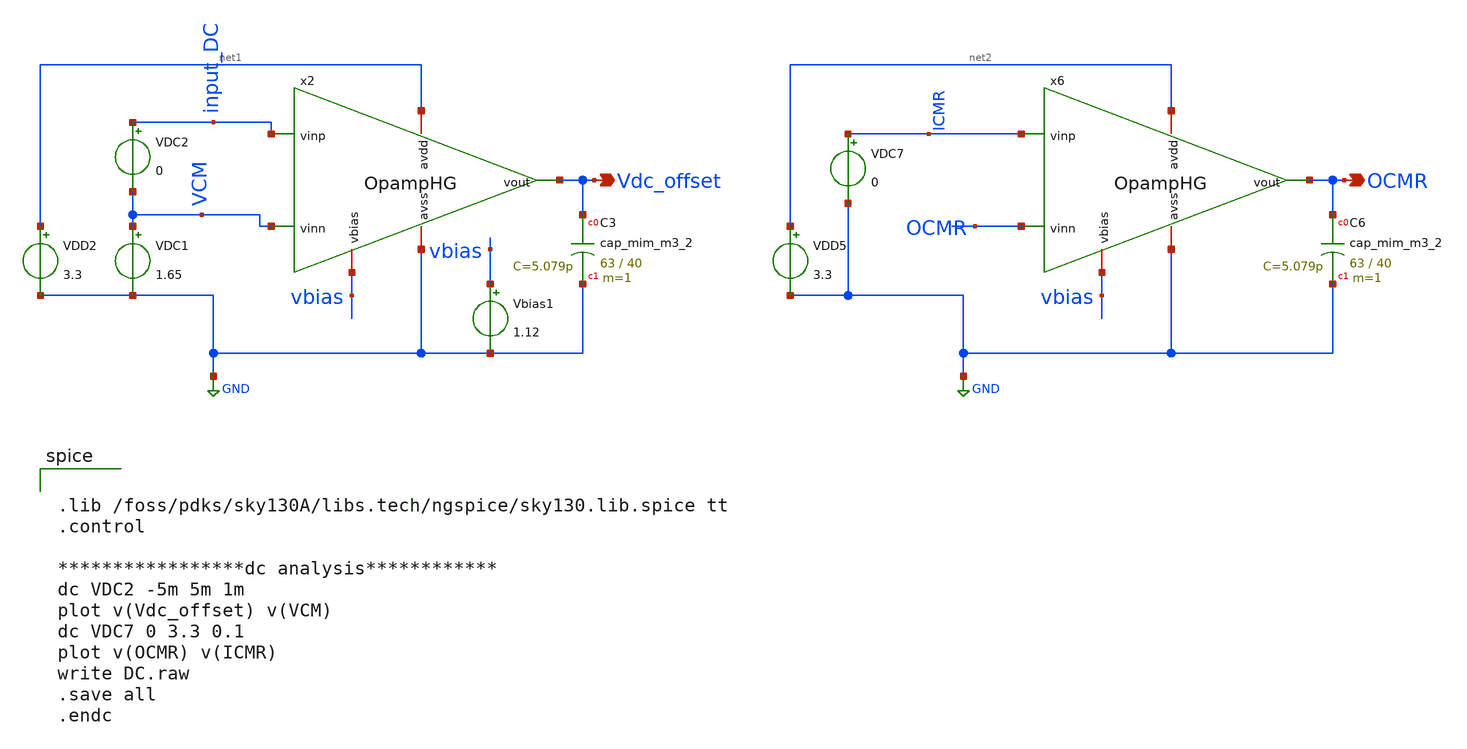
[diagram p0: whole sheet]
** sch_path: OpampHG_DC.sch
**.subckt OpampHG_DC Vdc_offset OCMR
*.opin Vdc_offset
*.opin OCMR
x2 net1 GND vbias input_DC VCM Vdc_offset OpampHG
VDD2 net1 GND 3.3
VDC1 VCM GND 1.65
XC3 Vdc_offset GND sky130_fd_pr__cap_mim_m3_2 W=63 L=40 MF=1 m=1
VDC2 input_DC VCM 0
x6 net2 GND vbias ICMR OCMR OCMR OpampHG
VDD5 net2 GND 3.3
VDC7 ICMR GND 0
XC6 OCMR GND sky130_fd_pr__cap_mim_m3_2 W=63 L=40 MF=1 m=1
Vbias1 vbias GND 1.12
**** begin user architecture code


.lib /foss/pdks/sky130A/libs.tech/ngspice/sky130.lib.spice tt
.control

*****************dc analysis************
dc VDC2 -5m 5m 1m
plot v(Vdc_offset) v(VCM)
dc VDC7 0 3.3 0.1
plot v(OCMR) v(ICMR)
write DC.raw
.save all
.endc


**** end user architecture code
**.ends

* expanding   symbol:  /foss/designs/Opamp_HG/OpampHG.sym # of pins=6
** sym_path: OpampHG.sym
** sch_path: OpampHG.sch
.subckt OpampHG avdd avss vbias vinp vinn vout
*.iopin avdd
*.iopin avss
*.iopin vbias
*.ipin vinp
*.ipin vinn
*.opin vout
XC1 net2 Vout_prior sky130_fd_pr__cap_mim_m3_1 W=13 L=9.9 MF=1 m=1
XC2 net3 vout sky130_fd_pr__cap_mim_m3_2 W=20 L=37 MF=1 m=1
XM1 net1 net2 avdd avdd sky130_fd_pr__pfet_01v8 L=0.3 W=5 nf=1 ad='int((nf+1)/2) * W/nf * 0.29' as='int((nf+2)/2) * W/nf * 0.29'
+ pd='2*int((nf+1)/2) * (W/nf + 0.29)' ps='2*int((nf+2)/2) * (W/nf + 0.29)' nrd='0.29 / W' nrs='0.29 / W'
+ sa=0 sb=0 sd=0 mult=1 m=1
XM2 net3 net2 avdd avdd sky130_fd_pr__pfet_01v8 L=0.3 W=5 nf=1 ad='int((nf+1)/2) * W/nf * 0.29' as='int((nf+2)/2) * W/nf * 0.29'
+ pd='2*int((nf+1)/2) * (W/nf + 0.29)' ps='2*int((nf+2)/2) * (W/nf + 0.29)' nrd='0.29 / W' nrs='0.29 / W'
+ sa=0 sb=0 sd=0 mult=1 m=1
XM3 net2 net2 net1 avdd sky130_fd_pr__pfet_01v8 L=0.3 W=5 nf=1 ad='int((nf+1)/2) * W/nf * 0.29' as='int((nf+2)/2) * W/nf * 0.29'
+ pd='2*int((nf+1)/2) * (W/nf + 0.29)' ps='2*int((nf+2)/2) * (W/nf + 0.29)' nrd='0.29 / W' nrs='0.29 / W'
+ sa=0 sb=0 sd=0 mult=1 m=1
XM4 net5 net2 net3 avdd sky130_fd_pr__pfet_01v8 L=0.3 W=5 nf=1 ad='int((nf+1)/2) * W/nf * 0.29' as='int((nf+2)/2) * W/nf * 0.29'
+ pd='2*int((nf+1)/2) * (W/nf + 0.29)' ps='2*int((nf+2)/2) * (W/nf + 0.29)' nrd='0.29 / W' nrs='0.29 / W'
+ sa=0 sb=0 sd=0 mult=1 m=1
XM5 net7 net6 avdd avdd sky130_fd_pr__pfet_01v8 L=0.3 W=5 nf=1 ad='int((nf+1)/2) * W/nf * 0.29' as='int((nf+2)/2) * W/nf * 0.29'
+ pd='2*int((nf+1)/2) * (W/nf + 0.29)' ps='2*int((nf+2)/2) * (W/nf + 0.29)' nrd='0.29 / W' nrs='0.29 / W'
+ sa=0 sb=0 sd=0 mult=1 m=1
XM6 net8 net6 avdd avdd sky130_fd_pr__pfet_01v8 L=0.3 W=5 nf=1 ad='int((nf+1)/2) * W/nf * 0.29' as='int((nf+2)/2) * W/nf * 0.29'
+ pd='2*int((nf+1)/2) * (W/nf + 0.29)' ps='2*int((nf+2)/2) * (W/nf + 0.29)' nrd='0.29 / W' nrs='0.29 / W'
+ sa=0 sb=0 sd=0 mult=1 m=1
XM7 net6 net6 net7 avdd sky130_fd_pr__pfet_01v8 L=0.3 W=5 nf=1 ad='int((nf+1)/2) * W/nf * 0.29' as='int((nf+2)/2) * W/nf * 0.29'
+ pd='2*int((nf+1)/2) * (W/nf + 0.29)' ps='2*int((nf+2)/2) * (W/nf + 0.29)' nrd='0.29 / W' nrs='0.29 / W'
+ sa=0 sb=0 sd=0 mult=1 m=1
XM8 Vout_prior net6 net8 avdd sky130_fd_pr__pfet_01v8 L=0.3 W=5 nf=1 ad='int((nf+1)/2) * W/nf * 0.29'
+ as='int((nf+2)/2) * W/nf * 0.29' pd='2*int((nf+1)/2) * (W/nf + 0.29)' ps='2*int((nf+2)/2) * (W/nf + 0.29)'
+ nrd='0.29 / W' nrs='0.29 / W' sa=0 sb=0 sd=0 mult=1 m=1
XM9 net11 Vout_prior avdd avdd sky130_fd_pr__pfet_01v8 L=0.3 W=50 nf=1 ad='int((nf+1)/2) * W/nf * 0.29'
+ as='int((nf+2)/2) * W/nf * 0.29' pd='2*int((nf+1)/2) * (W/nf + 0.29)' ps='2*int((nf+2)/2) * (W/nf + 0.29)'
+ nrd='0.29 / W' nrs='0.29 / W' sa=0 sb=0 sd=0 mult=1 m=1
XM10 vout Vout_prior net11 avdd sky130_fd_pr__pfet_01v8 L=0.3 W=50 nf=1 ad='int((nf+1)/2) * W/nf * 0.29'
+ as='int((nf+2)/2) * W/nf * 0.29' pd='2*int((nf+1)/2) * (W/nf + 0.29)' ps='2*int((nf+2)/2) * (W/nf + 0.29)'
+ nrd='0.29 / W' nrs='0.29 / W' sa=0 sb=0 sd=0 mult=1 m=1
XM11 net2 vinn net4 avss sky130_fd_pr__nfet_01v8 L=2 W=5 nf=1 ad='int((nf+1)/2) * W/nf * 0.29' as='int((nf+2)/2) * W/nf * 0.29'
+ pd='2*int((nf+1)/2) * (W/nf + 0.29)' ps='2*int((nf+2)/2) * (W/nf + 0.29)' nrd='0.29 / W' nrs='0.29 / W'
+ sa=0 sb=0 sd=0 mult=1 m=1
XM12 net5 vinp net4 avss sky130_fd_pr__nfet_01v8 L=2 W=5 nf=1 ad='int((nf+1)/2) * W/nf * 0.29' as='int((nf+2)/2) * W/nf * 0.29'
+ pd='2*int((nf+1)/2) * (W/nf + 0.29)' ps='2*int((nf+2)/2) * (W/nf + 0.29)' nrd='0.29 / W' nrs='0.29 / W'
+ sa=0 sb=0 sd=0 mult=1 m=1
XM13 net6 net5 net10 avss sky130_fd_pr__nfet_01v8 L=2 W=5 nf=1 ad='int((nf+1)/2) * W/nf * 0.29' as='int((nf+2)/2) * W/nf * 0.29'
+ pd='2*int((nf+1)/2) * (W/nf + 0.29)' ps='2*int((nf+2)/2) * (W/nf + 0.29)' nrd='0.29 / W' nrs='0.29 / W'
+ sa=0 sb=0 sd=0 mult=1 m=1
XM14 Vout_prior net2 net9 avss sky130_fd_pr__nfet_01v8 L=2 W=5 nf=1 ad='int((nf+1)/2) * W/nf * 0.29'
+ as='int((nf+2)/2) * W/nf * 0.29' pd='2*int((nf+1)/2) * (W/nf + 0.29)' ps='2*int((nf+2)/2) * (W/nf + 0.29)'
+ nrd='0.29 / W' nrs='0.29 / W' sa=0 sb=0 sd=0 mult=1 m=1
XM15 net4 vbias avss avss sky130_fd_pr__nfet_01v8 L=0.6 W=2.6 nf=1 ad='int((nf+1)/2) * W/nf * 0.29' as='int((nf+2)/2) * W/nf * 0.29'
+ pd='2*int((nf+1)/2) * (W/nf + 0.29)' ps='2*int((nf+2)/2) * (W/nf + 0.29)' nrd='0.29 / W' nrs='0.29 / W'
+ sa=0 sb=0 sd=0 mult=1 m=1
XM16 net4 vbias avss avss sky130_fd_pr__nfet_01v8 L=0.6 W=2.6 nf=1 ad='int((nf+1)/2) * W/nf * 0.29' as='int((nf+2)/2) * W/nf * 0.29'
+ pd='2*int((nf+1)/2) * (W/nf + 0.29)' ps='2*int((nf+2)/2) * (W/nf + 0.29)' nrd='0.29 / W' nrs='0.29 / W'
+ sa=0 sb=0 sd=0 mult=1 m=1
XM17 net10 vbias avss avss sky130_fd_pr__nfet_01v8 L=0.6 W=2.6 nf=1 ad='int((nf+1)/2) * W/nf * 0.29'
+ as='int((nf+2)/2) * W/nf * 0.29' pd='2*int((nf+1)/2) * (W/nf + 0.29)' ps='2*int((nf+2)/2) * (W/nf + 0.29)'
+ nrd='0.29 / W' nrs='0.29 / W' sa=0 sb=0 sd=0 mult=1 m=1
XM18 net9 vbias avss avss sky130_fd_pr__nfet_01v8 L=0.6 W=2.6 nf=1 ad='int((nf+1)/2) * W/nf * 0.29' as='int((nf+2)/2) * W/nf * 0.29'
+ pd='2*int((nf+1)/2) * (W/nf + 0.29)' ps='2*int((nf+2)/2) * (W/nf + 0.29)' nrd='0.29 / W' nrs='0.29 / W'
+ sa=0 sb=0 sd=0 mult=1 m=1
XM19 vout vbias avss avss sky130_fd_pr__nfet_01v8 L=0.6 W=20.4 nf=1 ad='int((nf+1)/2) * W/nf * 0.29'
+ as='int((nf+2)/2) * W/nf * 0.29' pd='2*int((nf+1)/2) * (W/nf + 0.29)' ps='2*int((nf+2)/2) * (W/nf + 0.29)'
+ nrd='0.29 / W' nrs='0.29 / W' sa=0 sb=0 sd=0 mult=1 m=1
.ends

.GLOBAL GND
.end
